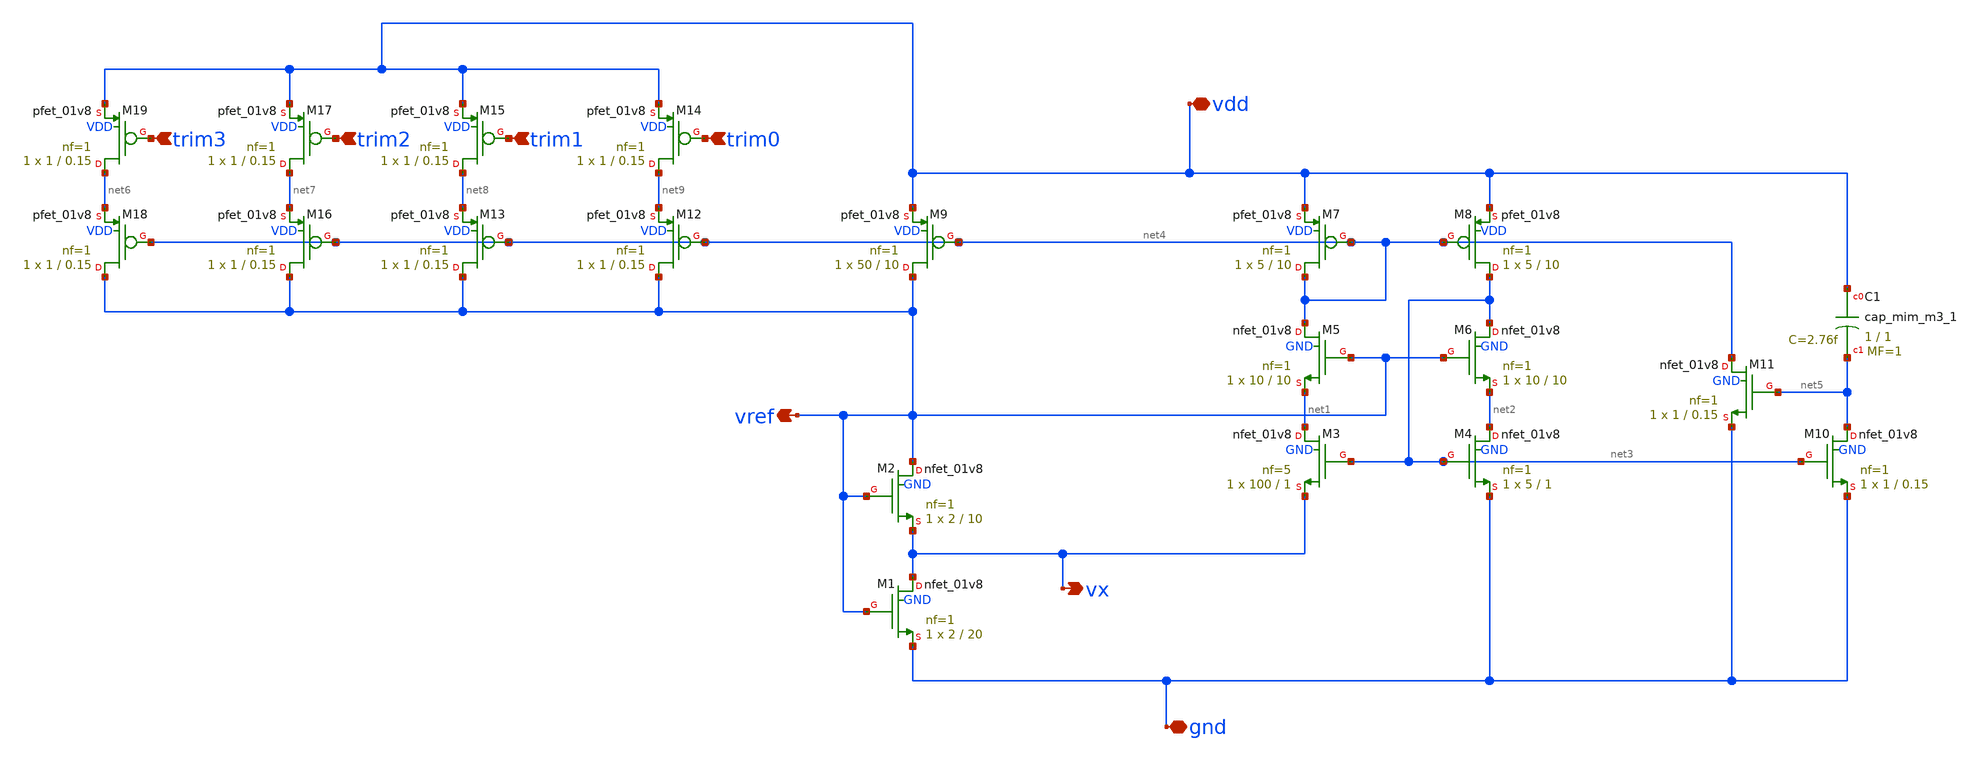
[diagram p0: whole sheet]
** sch_path: xschem/cmos_vref.sch
**.subckt cmos_vref vref gnd vdd vx trim0 trim1 trim2 trim3
*.opin vref
*.iopin gnd
*.iopin vdd
*.opin vx
*.ipin trim0
*.ipin trim1
*.ipin trim2
*.ipin trim3
XM2 vref vref vx GND sky130_fd_pr__nfet_01v8 L=10 W=2 nf=1 ad='int((nf+1)/2) * W/nf * 0.29' as='int((nf+2)/2) * W/nf * 0.29'
+ pd='2*int((nf+1)/2) * (W/nf + 0.29)' ps='2*int((nf+2)/2) * (W/nf + 0.29)' nrd='0.29 / W' nrs='0.29 / W'
+ sa=0 sb=0 sd=0 mult=1 m=1
XM1 vx vref gnd GND sky130_fd_pr__nfet_01v8 L=20 W=2 nf=1 ad='int((nf+1)/2) * W/nf * 0.29' as='int((nf+2)/2) * W/nf * 0.29'
+ pd='2*int((nf+1)/2) * (W/nf + 0.29)' ps='2*int((nf+2)/2) * (W/nf + 0.29)' nrd='0.29 / W' nrs='0.29 / W'
+ sa=0 sb=0 sd=0 mult=1 m=1
XM3 net1 net3 vx GND sky130_fd_pr__nfet_01v8 L=1 W=100 nf=5 ad='int((nf+1)/2) * W/nf * 0.29' as='int((nf+2)/2) * W/nf * 0.29'
+ pd='2*int((nf+1)/2) * (W/nf + 0.29)' ps='2*int((nf+2)/2) * (W/nf + 0.29)' nrd='0.29 / W' nrs='0.29 / W'
+ sa=0 sb=0 sd=0 mult=1 m=1
XM4 net2 net3 gnd GND sky130_fd_pr__nfet_01v8 L=1 W=5 nf=1 ad='int((nf+1)/2) * W/nf * 0.29' as='int((nf+2)/2) * W/nf * 0.29'
+ pd='2*int((nf+1)/2) * (W/nf + 0.29)' ps='2*int((nf+2)/2) * (W/nf + 0.29)' nrd='0.29 / W' nrs='0.29 / W'
+ sa=0 sb=0 sd=0 mult=1 m=1
XM5 net4 vref net1 GND sky130_fd_pr__nfet_01v8 L=10 W=10 nf=1 ad='int((nf+1)/2) * W/nf * 0.29' as='int((nf+2)/2) * W/nf * 0.29'
+ pd='2*int((nf+1)/2) * (W/nf + 0.29)' ps='2*int((nf+2)/2) * (W/nf + 0.29)' nrd='0.29 / W' nrs='0.29 / W'
+ sa=0 sb=0 sd=0 mult=1 m=1
XM6 net3 vref net2 GND sky130_fd_pr__nfet_01v8 L=10 W=10 nf=1 ad='int((nf+1)/2) * W/nf * 0.29' as='int((nf+2)/2) * W/nf * 0.29'
+ pd='2*int((nf+1)/2) * (W/nf + 0.29)' ps='2*int((nf+2)/2) * (W/nf + 0.29)' nrd='0.29 / W' nrs='0.29 / W'
+ sa=0 sb=0 sd=0 mult=1 m=1
XM7 net4 net4 vdd VDD sky130_fd_pr__pfet_01v8 L=10 W=5 nf=1 ad='int((nf+1)/2) * W/nf * 0.29' as='int((nf+2)/2) * W/nf * 0.29'
+ pd='2*int((nf+1)/2) * (W/nf + 0.29)' ps='2*int((nf+2)/2) * (W/nf + 0.29)' nrd='0.29 / W' nrs='0.29 / W'
+ sa=0 sb=0 sd=0 mult=1 m=1
XM8 net3 net4 vdd VDD sky130_fd_pr__pfet_01v8 L=10 W=5 nf=1 ad='int((nf+1)/2) * W/nf * 0.29' as='int((nf+2)/2) * W/nf * 0.29'
+ pd='2*int((nf+1)/2) * (W/nf + 0.29)' ps='2*int((nf+2)/2) * (W/nf + 0.29)' nrd='0.29 / W' nrs='0.29 / W'
+ sa=0 sb=0 sd=0 mult=1 m=1
XM9 vref net4 vdd VDD sky130_fd_pr__pfet_01v8 L=10 W=50 nf=1 ad='int((nf+1)/2) * W/nf * 0.29' as='int((nf+2)/2) * W/nf * 0.29'
+ pd='2*int((nf+1)/2) * (W/nf + 0.29)' ps='2*int((nf+2)/2) * (W/nf + 0.29)' nrd='0.29 / W' nrs='0.29 / W'
+ sa=0 sb=0 sd=0 mult=1 m=1
XM10 net5 net3 gnd GND sky130_fd_pr__nfet_01v8 L=0.15 W=1 nf=1 ad='int((nf+1)/2) * W/nf * 0.29' as='int((nf+2)/2) * W/nf * 0.29'
+ pd='2*int((nf+1)/2) * (W/nf + 0.29)' ps='2*int((nf+2)/2) * (W/nf + 0.29)' nrd='0.29 / W' nrs='0.29 / W'
+ sa=0 sb=0 sd=0 mult=1 m=1
XM11 net4 net5 gnd GND sky130_fd_pr__nfet_01v8 L=0.15 W=1 nf=1 ad='int((nf+1)/2) * W/nf * 0.29' as='int((nf+2)/2) * W/nf * 0.29'
+ pd='2*int((nf+1)/2) * (W/nf + 0.29)' ps='2*int((nf+2)/2) * (W/nf + 0.29)' nrd='0.29 / W' nrs='0.29 / W'
+ sa=0 sb=0 sd=0 mult=1 m=1
XC1 vdd net5 sky130_fd_pr__cap_mim_m3_1 W=1 L=1 MF=1 m=1
XM12 vref net4 net9 VDD sky130_fd_pr__pfet_01v8 L=0.15 W=1 nf=1 ad='int((nf+1)/2) * W/nf * 0.29' as='int((nf+2)/2) * W/nf * 0.29'
+ pd='2*int((nf+1)/2) * (W/nf + 0.29)' ps='2*int((nf+2)/2) * (W/nf + 0.29)' nrd='0.29 / W' nrs='0.29 / W'
+ sa=0 sb=0 sd=0 mult=1 m=1
XM13 vref net4 net8 VDD sky130_fd_pr__pfet_01v8 L=0.15 W=1 nf=1 ad='int((nf+1)/2) * W/nf * 0.29' as='int((nf+2)/2) * W/nf * 0.29'
+ pd='2*int((nf+1)/2) * (W/nf + 0.29)' ps='2*int((nf+2)/2) * (W/nf + 0.29)' nrd='0.29 / W' nrs='0.29 / W'
+ sa=0 sb=0 sd=0 mult=1 m=1
XM14 net9 trim0 vdd VDD sky130_fd_pr__pfet_01v8 L=0.15 W=1 nf=1 ad='int((nf+1)/2) * W/nf * 0.29' as='int((nf+2)/2) * W/nf * 0.29'
+ pd='2*int((nf+1)/2) * (W/nf + 0.29)' ps='2*int((nf+2)/2) * (W/nf + 0.29)' nrd='0.29 / W' nrs='0.29 / W'
+ sa=0 sb=0 sd=0 mult=1 m=1
XM15 net8 trim1 vdd VDD sky130_fd_pr__pfet_01v8 L=0.15 W=1 nf=1 ad='int((nf+1)/2) * W/nf * 0.29' as='int((nf+2)/2) * W/nf * 0.29'
+ pd='2*int((nf+1)/2) * (W/nf + 0.29)' ps='2*int((nf+2)/2) * (W/nf + 0.29)' nrd='0.29 / W' nrs='0.29 / W'
+ sa=0 sb=0 sd=0 mult=1 m=1
XM16 vref net4 net7 VDD sky130_fd_pr__pfet_01v8 L=0.15 W=1 nf=1 ad='int((nf+1)/2) * W/nf * 0.29' as='int((nf+2)/2) * W/nf * 0.29'
+ pd='2*int((nf+1)/2) * (W/nf + 0.29)' ps='2*int((nf+2)/2) * (W/nf + 0.29)' nrd='0.29 / W' nrs='0.29 / W'
+ sa=0 sb=0 sd=0 mult=1 m=1
XM17 net7 trim2 vdd VDD sky130_fd_pr__pfet_01v8 L=0.15 W=1 nf=1 ad='int((nf+1)/2) * W/nf * 0.29' as='int((nf+2)/2) * W/nf * 0.29'
+ pd='2*int((nf+1)/2) * (W/nf + 0.29)' ps='2*int((nf+2)/2) * (W/nf + 0.29)' nrd='0.29 / W' nrs='0.29 / W'
+ sa=0 sb=0 sd=0 mult=1 m=1
XM18 vref net4 net6 VDD sky130_fd_pr__pfet_01v8 L=0.15 W=1 nf=1 ad='int((nf+1)/2) * W/nf * 0.29' as='int((nf+2)/2) * W/nf * 0.29'
+ pd='2*int((nf+1)/2) * (W/nf + 0.29)' ps='2*int((nf+2)/2) * (W/nf + 0.29)' nrd='0.29 / W' nrs='0.29 / W'
+ sa=0 sb=0 sd=0 mult=1 m=1
XM19 net6 trim3 vdd VDD sky130_fd_pr__pfet_01v8 L=0.15 W=1 nf=1 ad='int((nf+1)/2) * W/nf * 0.29' as='int((nf+2)/2) * W/nf * 0.29'
+ pd='2*int((nf+1)/2) * (W/nf + 0.29)' ps='2*int((nf+2)/2) * (W/nf + 0.29)' nrd='0.29 / W' nrs='0.29 / W'
+ sa=0 sb=0 sd=0 mult=1 m=1
**.ends
.end
